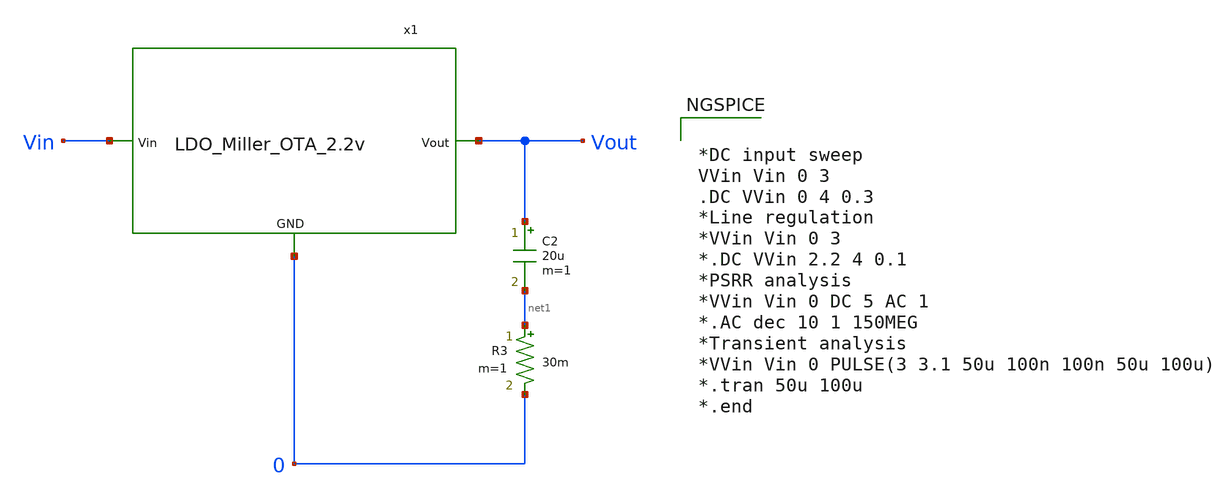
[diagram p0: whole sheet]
** sch_path: Analog_Blocks/LDO/Testbench/LDO_Miller_2.2v_TB.sch
**.subckt LDO_Miller_2.2v_TB
C2 Vout net1 20u m=1
R3 net1 0 30m m=1
x1 Vin Vout 0 LDO_Miller_OTA_2.2v
**** begin user architecture code


*DC input sweep
VVin Vin 0 3
.DC VVin 0 4 0.3
*Line regulation
*VVin Vin 0 3
*.DC VVin 2.2 4 0.1
*PSRR analysis
*VVin Vin 0 DC 5 AC 1
*.AC dec 10 1 150MEG
*Transient analysis
*VVin Vin 0 PULSE(3 3.1 50u 100n 100n 50u 100u)
*.tran 50u 100u
*.end



.include $::SKYWATER_MODELS/cells/nfet_01v8/sky130_fd_pr__nfet_01v8__tt.corner.spice
.include $::SKYWATER_MODELS/cells/nfet_01v8_lvt/sky130_fd_pr__nfet_01v8_lvt__tt.corner.spice
.include $::SKYWATER_MODELS/cells/pfet_01v8/sky130_fd_pr__pfet_01v8__tt.corner.spice
.include $::SKYWATER_MODELS/cells/nfet_03v3_nvt/sky130_fd_pr__nfet_03v3_nvt__tt.corner.spice
.include $::SKYWATER_MODELS/cells/nfet_05v0_nvt/sky130_fd_pr__nfet_05v0_nvt__tt.corner.spice
.include $::SKYWATER_MODELS/cells/esd_nfet_01v8/sky130_fd_pr__esd_nfet_01v8__tt.corner.spice
.include $::SKYWATER_MODELS/cells/pfet_01v8_lvt/sky130_fd_pr__pfet_01v8_lvt__tt.corner.spice
.include $::SKYWATER_MODELS/cells/pfet_01v8_hvt/sky130_fd_pr__pfet_01v8_hvt__tt.corner.spice
.include $::SKYWATER_MODELS/cells/esd_pfet_g5v0d10v5/sky130_fd_pr__esd_pfet_g5v0d10v5__tt.corner.spice
.include $::SKYWATER_MODELS/cells/pfet_g5v0d10v5/sky130_fd_pr__pfet_g5v0d10v5__tt.corner.spice
.include $::SKYWATER_MODELS/cells/pfet_g5v0d16v0/sky130_fd_pr__pfet_g5v0d16v0__tt.corner.spice
.include $::SKYWATER_MODELS/cells/nfet_g5v0d10v5/sky130_fd_pr__nfet_g5v0d10v5__tt.corner.spice
.include $::SKYWATER_MODELS/cells/nfet_g5v0d16v0/sky130_fd_pr__nfet_g5v0d16v0__tt_discrete.corner.spice
.include $::SKYWATER_MODELS/cells/esd_nfet_g5v0d10v5/sky130_fd_pr__esd_nfet_g5v0d10v5__tt.corner.spice
.include $::SKYWATER_MODELS/models/corners/tt/nonfet.spice
* Mismatch parameters
.include $::SKYWATER_MODELS/cells/nfet_01v8/sky130_fd_pr__nfet_01v8__mismatch.corner.spice
.include $::SKYWATER_MODELS/cells/pfet_01v8/sky130_fd_pr__pfet_01v8__mismatch.corner.spice
.include $::SKYWATER_MODELS/cells/nfet_01v8_lvt/sky130_fd_pr__nfet_01v8_lvt__mismatch.corner.spice
.include $::SKYWATER_MODELS/cells/pfet_01v8_lvt/sky130_fd_pr__pfet_01v8_lvt__mismatch.corner.spice
.include $::SKYWATER_MODELS/cells/pfet_01v8_hvt/sky130_fd_pr__pfet_01v8_hvt__mismatch.corner.spice
.include $::SKYWATER_MODELS/cells/nfet_g5v0d10v5/sky130_fd_pr__nfet_g5v0d10v5__mismatch.corner.spice
.include $::SKYWATER_MODELS/cells/pfet_g5v0d10v5/sky130_fd_pr__pfet_g5v0d10v5__mismatch.corner.spice
.include $::SKYWATER_MODELS/cells/nfet_05v0_nvt/sky130_fd_pr__nfet_05v0_nvt__mismatch.corner.spice
.include $::SKYWATER_MODELS/cells/nfet_03v3_nvt/sky130_fd_pr__nfet_03v3_nvt__mismatch.corner.spice
* Resistor$::SKYWATER_MODELS/Capacitor
.include $::SKYWATER_MODELS/models/r+c/res_typical__cap_typical.spice
.include $::SKYWATER_MODELS/models/r+c/res_typical__cap_typical__lin.spice
* Special cells
.include $::SKYWATER_MODELS/models/corners/tt/specialized_cells.spice
* All models
.include $::SKYWATER_MODELS/models/all.spice
* Corner
.include $::SKYWATER_MODELS/models/corners/tt/rf.spice

**** end user architecture code
**.ends
.end
